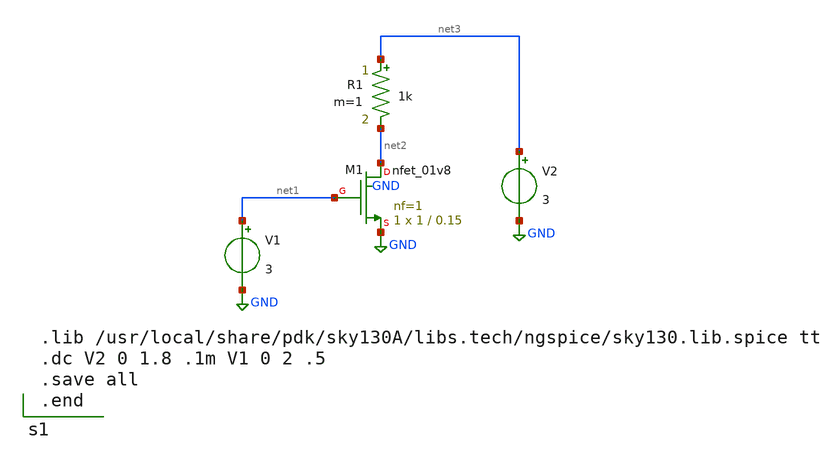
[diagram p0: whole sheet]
** sch_path: XSCHEM/nmos_drain_current/nmos.sch
* Copyright 2021 Stefan Frederik Schippers
* Licensed under the Apache License, Version 2.0 (the "License");
* you may not use this file except in compliance with the License.
* You may obtain a copy of the License at
* https://www.apache.org/licenses/LICENSE-2.0
* Unless required by applicable law or agreed to in writing, software
* distributed under the License is distributed on an "AS IS" BASIS,
* WITHOUT WARRANTIES OR CONDITIONS OF ANY KIND, either express or implied.
* See the License for the specific language governing permissions and
* limitations under the License.
**.subckt nmos
XM1 net2 net1 GND GND sky130_fd_pr__nfet_01v8 L=0.15 W=1 nf=1 ad='int((nf+1)/2) * W/nf * 0.29' as='int((nf+2)/2) * W/nf * 0.29'
+ pd='2*int((nf+1)/2) * (W/nf + 0.29)' ps='2*int((nf+2)/2) * (W/nf + 0.29)' nrd='0.29 / W' nrs='0.29 / W'
+ sa=0 sb=0 sd=0 mult=1 m=1
R1 net3 net2 1k m=1
V1 net1 GND 3
V2 net3 GND 3
**** begin user architecture code

.lib /usr/local/share/pdk/sky130A/libs.tech/ngspice/sky130.lib.spice tt
.dc V2 0 1.8 .1m V1 0 2 .5
.save all
.end

**** end user architecture code
**.ends
.GLOBAL GND
.end
